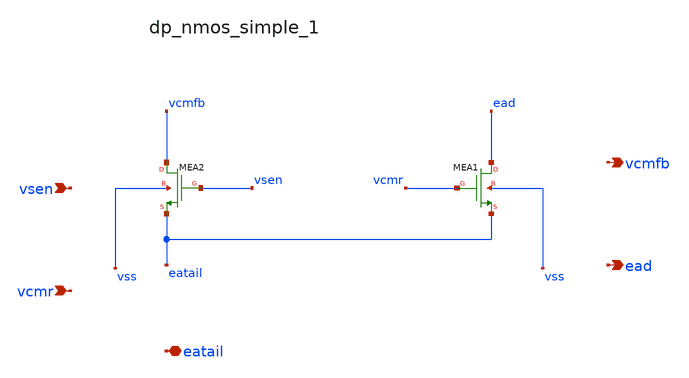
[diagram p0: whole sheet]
** sch_path: analog-db/raw/amp_023_fer_fd2s/hier/blocks/dp_nmos_simple_1.sch
**.subckt dp_nmos_simple_1 vsen vcmr eatail vcmfb ead
*.ipin vsen
*.ipin vcmr
*.iopin eatail
*.opin vcmfb
*.opin ead
XMEA1 ead vcmr eatail vss sg13_lv_nmos w=x_dut_xmea1_w l=x_dut_xmea1_l ng=1 m=x_dut_xmea1_m
XMEA2 vcmfb vsen eatail vss sg13_lv_nmos w=x_dut_xmea2_w l=x_dut_xmea2_l ng=1 m=x_dut_xmea2_m
**.ends
.end
